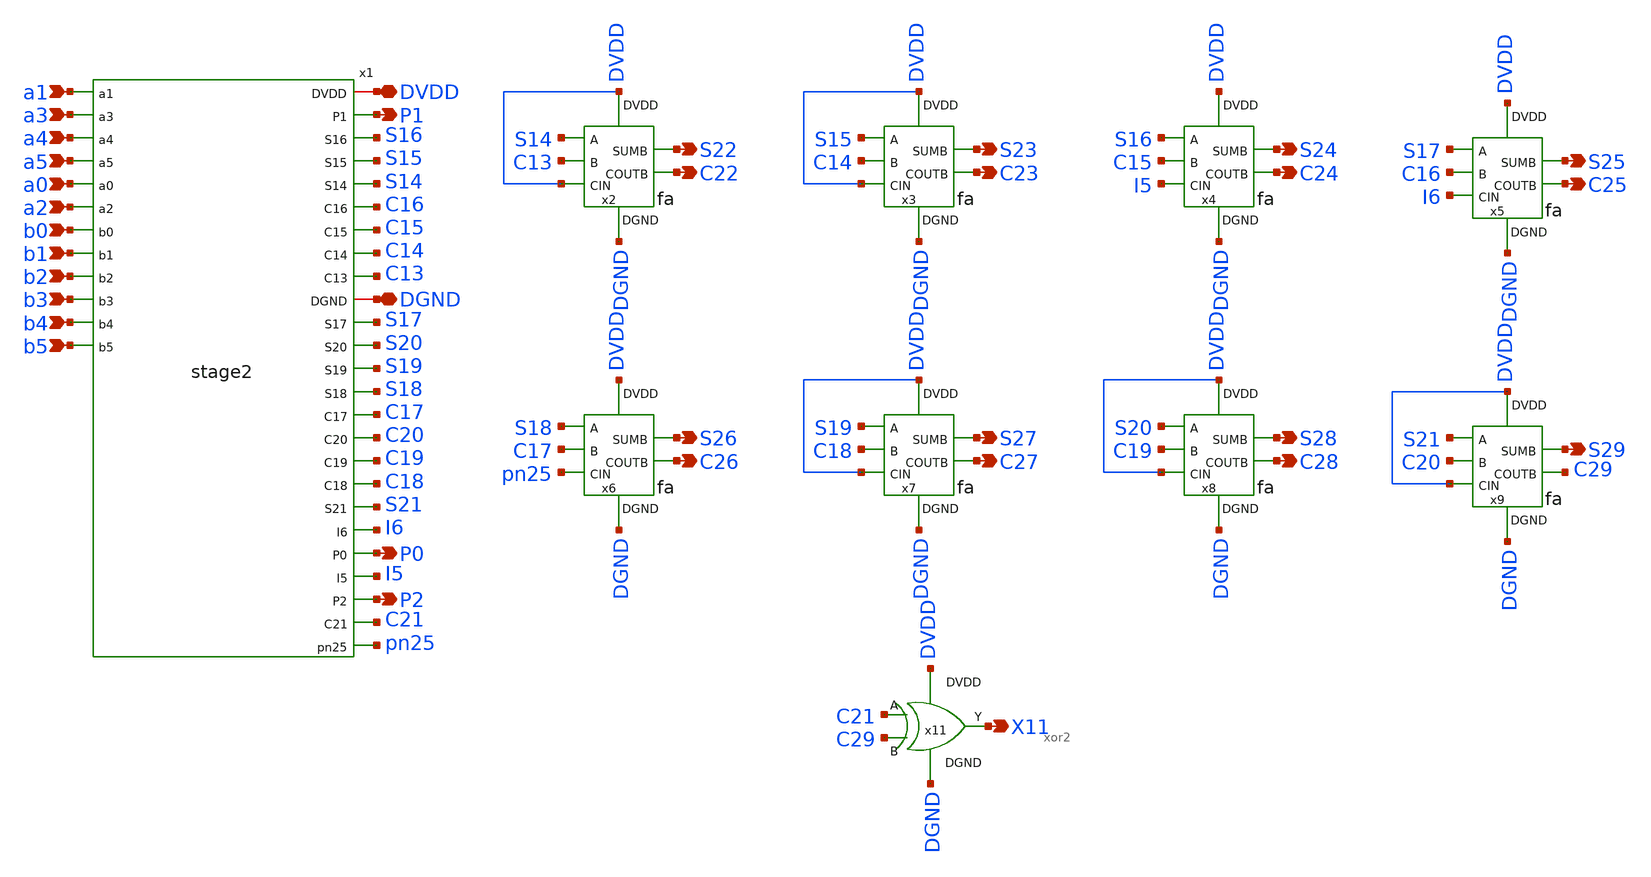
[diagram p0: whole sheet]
** sch_path: xschem/stage3.sch
**.subckt stage3 a1 a3 a4 a5 a0 a2 b0 b1 b2 b3 b4 b5 P1 P0 P2 C22 S23 C23 S24 C24 S25 C25 S26 C26
*+ S27 C27 S28 C28 S29 X11 S22 DVDD DGND
*.ipin a1
*.ipin a3
*.ipin a4
*.ipin a5
*.ipin a0
*.ipin a2
*.ipin b0
*.ipin b1
*.ipin b2
*.ipin b3
*.ipin b4
*.ipin b5
*.opin P1
*.opin P0
*.opin P2
*.opin C22
*.opin S23
*.opin C23
*.opin S24
*.opin C24
*.opin S25
*.opin C25
*.opin S26
*.opin C26
*.opin S27
*.opin C27
*.opin S28
*.opin C28
*.opin S29
*.opin X11
*.opin S22
*.iopin DVDD
*.iopin DGND
x2 DVDD DGND S14 C13 DVDD C22 S22 fa
x3 DVDD DGND S15 C14 DVDD C23 S23 fa
x4 DVDD DGND S16 C15 I5 C24 S24 fa
x5 DVDD DGND S17 C16 I6 C25 S25 fa
x6 DVDD DGND S18 C17 pn25 C26 S26 fa
x7 DVDD DGND S19 C18 DVDD C27 S27 fa
x8 DVDD DGND S20 C19 DVDD C28 S28 fa
x9 DVDD DGND S21 C20 DVDD C29 S29 fa
x11 DVDD C21 C29 X11 DGND xor2
x1 DVDD a1 a3 P1 a4 S16 S15 S14 a5 C16 C15 C14 C13 a0 a2 b0 b1 b2 DGND b3 b4 b5 S17 S20 S19 S18 C17
+ C20 C19 C18 S21 I6 P0 I5 P2 C21 pn25 stage2
**.ends
.end
